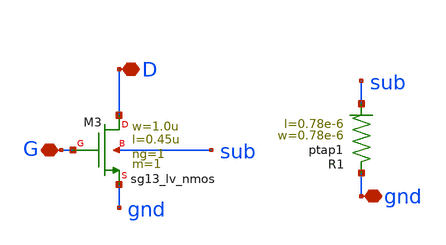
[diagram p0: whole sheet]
** sch_path: modules/module_0_foundations/lvs_tester/schematic/lvs_tester.sch
**.subckt lvs_tester G D gnd
*.iopin G
*.iopin D
*.iopin gnd
XM3 D G gnd sub sg13_lv_nmos w=1.0u l=0.45u ng=1 m=1 mm_ok=1
XR1 gnd sub ptap1 R=262.8 w=0.78e-6 l=0.78e-6
**.ends
.end
